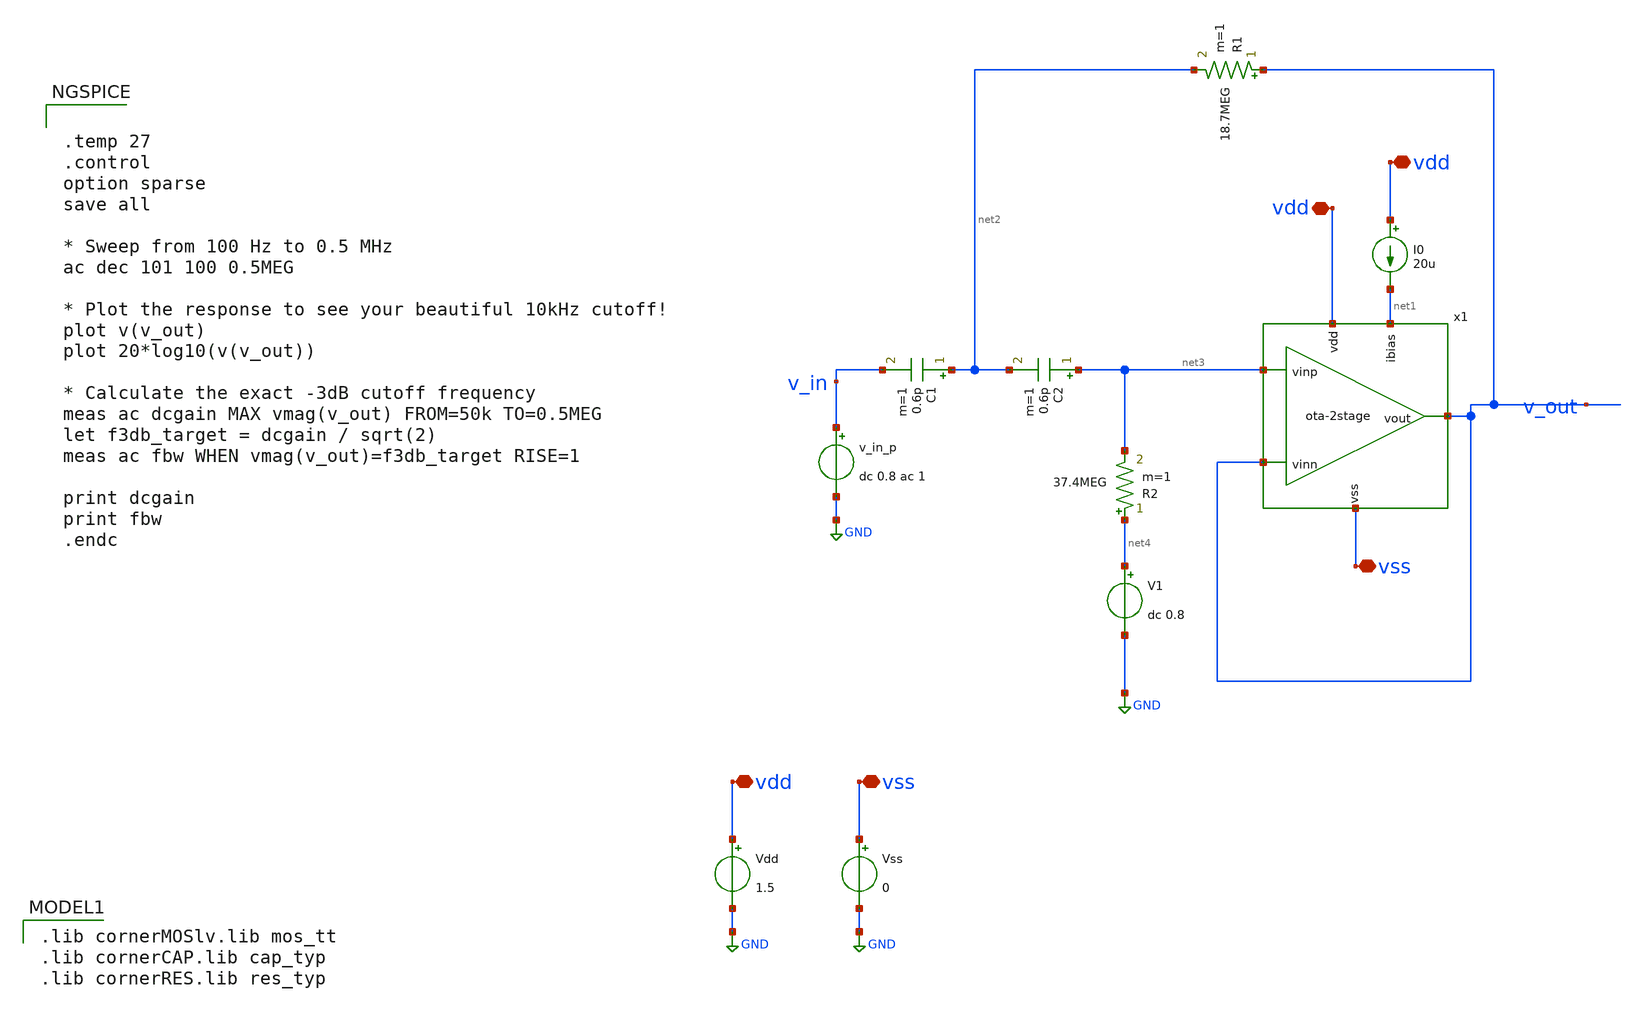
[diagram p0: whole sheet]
** sch_path: testbench/ota-2stage_tb-sk-hpf.sch
**.subckt ota-2stage_tb-sk-hpf vdd vdd vdd vss vss
*.iopin vdd
*.iopin vdd
*.iopin vdd
*.iopin vss
*.iopin vss
I0 vdd net1 20u
Vdd vdd GND 1.5
Vss vss GND 0
v_in_p v_in GND dc 0.8 ac 1
x1 vdd net1 v_out v_out net3 vss ota-2stage
R1 v_out net2 18.7MEG m=1
R2 net4 net3 37.4MEG m=1
C1 net2 v_in 0.6p m=1
C2 net3 net2 0.6p m=1
V1 net4 GND dc 0.8
**** begin user architecture code


.temp 27
.control
option sparse
save all

* Sweep from 100 Hz to 0.5 MHz
ac dec 101 100 0.5MEG

* Plot the response to see your beautiful 10kHz cutoff!
plot v(v_out)
plot 20*log10(v(v_out))

* Calculate the exact -3dB cutoff frequency
meas ac dcgain MAX vmag(v_out) FROM=50k TO=0.5MEG
let f3db_target = dcgain / sqrt(2)
meas ac fbw WHEN vmag(v_out)=f3db_target RISE=1

print dcgain
print fbw
.endc


 .lib cornerMOSlv.lib mos_tt
.lib cornerCAP.lib cap_typ
.lib cornerRES.lib res_typ

**** end user architecture code
**.ends
.GLOBAL GND
.end
